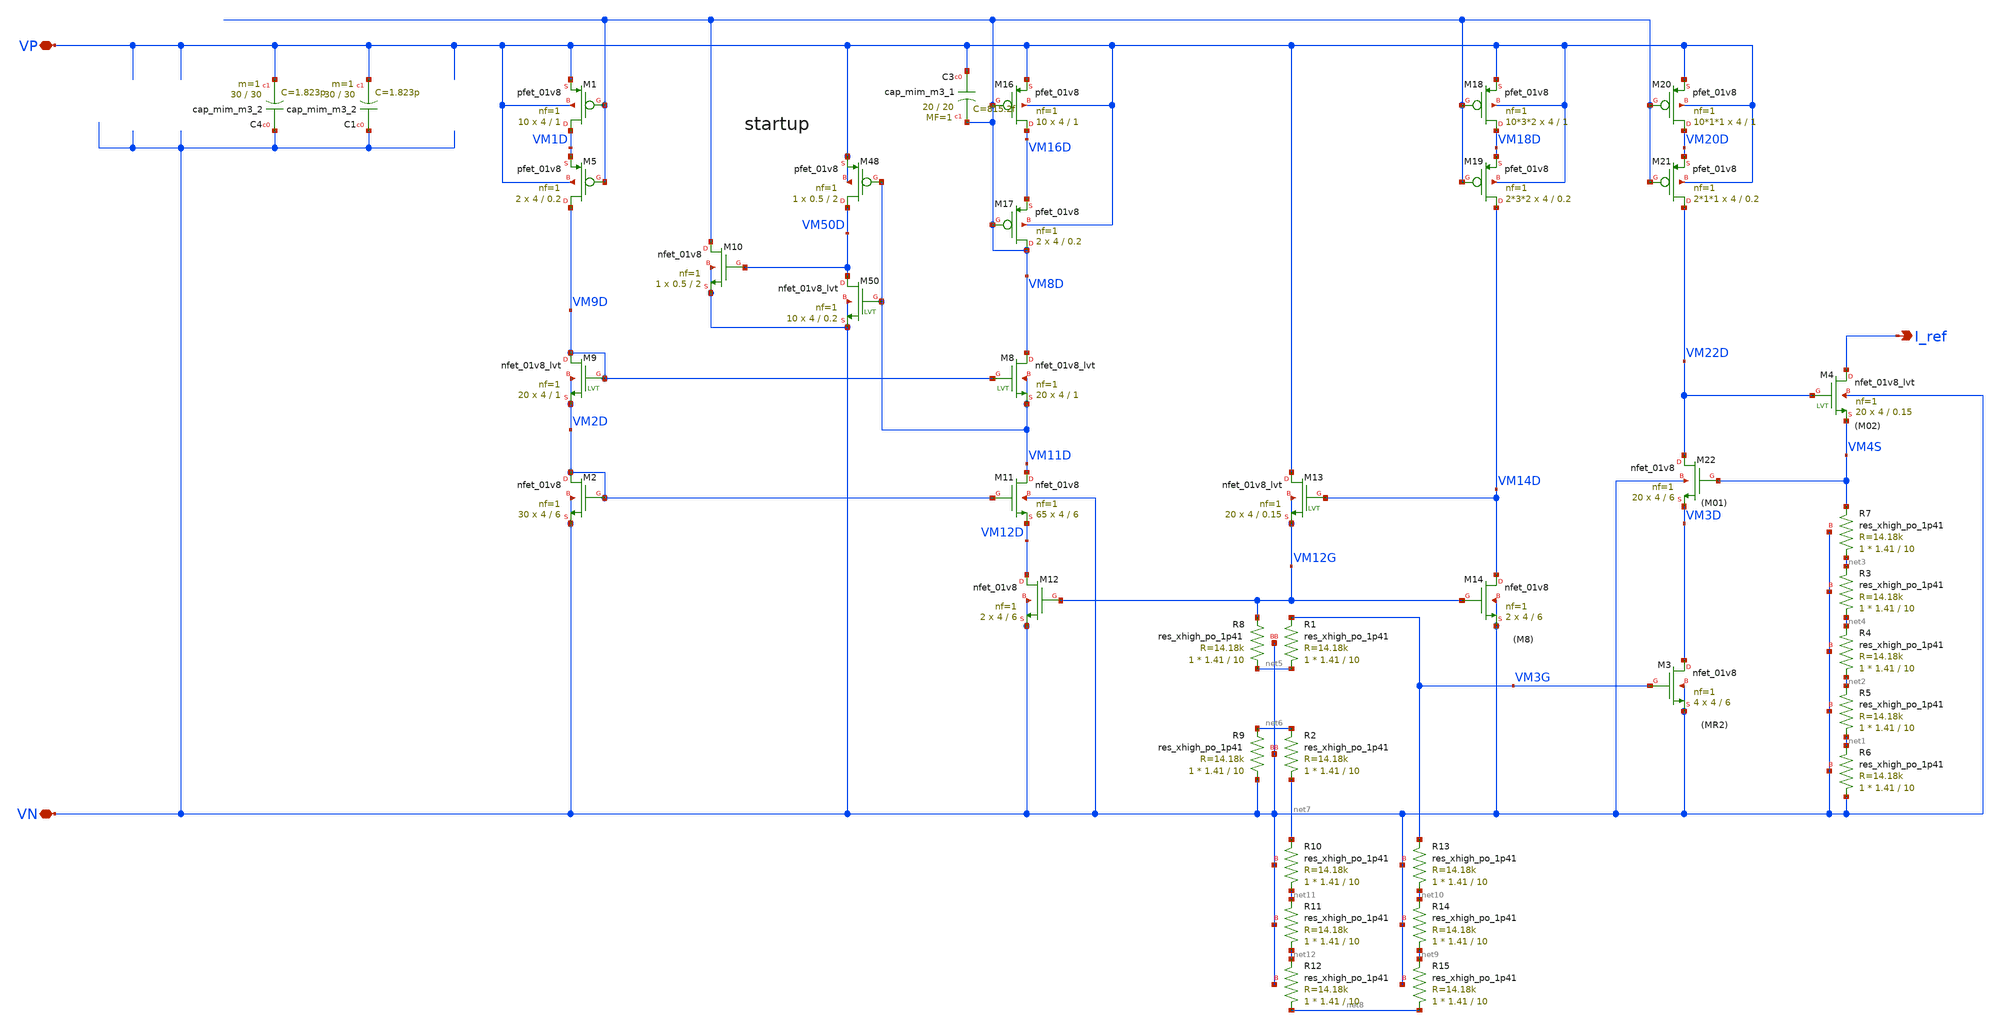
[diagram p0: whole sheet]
** sch_path: xschem/bias/low_pvt_source.sch
**.subckt low_pvt_source VP I_ref VN
*.iopin VP
*.opin I_ref
*.iopin VN
XM1 VM1D VM8D VP VP sky130_fd_pr__pfet_01v8 L=1 W=4 nf=1 ad='int((nf+1)/2) * W/nf * 0.29' as='int((nf+2)/2) * W/nf * 0.29'
+ pd='2*int((nf+1)/2) * (W/nf + 0.29)' ps='2*int((nf+2)/2) * (W/nf + 0.29)' nrd='0.29 / W' nrs='0.29 / W'
+ sa=0 sb=0 sd=0 mult=10 m=10
XM2 VM2D VM2D VN VN sky130_fd_pr__nfet_01v8 L=6 W=4 nf=1 ad='int((nf+1)/2) * W/nf * 0.29' as='int((nf+2)/2) * W/nf * 0.29'
+ pd='2*int((nf+1)/2) * (W/nf + 0.29)' ps='2*int((nf+2)/2) * (W/nf + 0.29)' nrd='0.29 / W' nrs='0.29 / W'
+ sa=0 sb=0 sd=0 mult=30 m=30
XM5 VM9D VM8D VM1D VP sky130_fd_pr__pfet_01v8 L=0.2 W=4 nf=1 ad='int((nf+1)/2) * W/nf * 0.29' as='int((nf+2)/2) * W/nf * 0.29'
+ pd='2*int((nf+1)/2) * (W/nf + 0.29)' ps='2*int((nf+2)/2) * (W/nf + 0.29)' nrd='0.29 / W' nrs='0.29 / W'
+ sa=0 sb=0 sd=0 mult=2 m=2
XM11 VM11D VM2D VM12D VN sky130_fd_pr__nfet_01v8 L=6 W=4 nf=1 ad='int((nf+1)/2) * W/nf * 0.29' as='int((nf+2)/2) * W/nf * 0.29'
+ pd='2*int((nf+1)/2) * (W/nf + 0.29)' ps='2*int((nf+2)/2) * (W/nf + 0.29)' nrd='0.29 / W' nrs='0.29 / W'
+ sa=0 sb=0 sd=0 mult=65 m=65
XM12 VM12D VM12G VN VN sky130_fd_pr__nfet_01v8 L=6 W=4 nf=1 ad='int((nf+1)/2) * W/nf * 0.29' as='int((nf+2)/2) * W/nf * 0.29'
+ pd='2*int((nf+1)/2) * (W/nf + 0.29)' ps='2*int((nf+2)/2) * (W/nf + 0.29)' nrd='0.29 / W' nrs='0.29 / W'
+ sa=0 sb=0 sd=0 mult=2 m=2
XM14 VM14D VM12G VN VN sky130_fd_pr__nfet_01v8 L=6 W=4 nf=1 ad='int((nf+1)/2) * W/nf * 0.29' as='int((nf+2)/2) * W/nf * 0.29'
+ pd='2*int((nf+1)/2) * (W/nf + 0.29)' ps='2*int((nf+2)/2) * (W/nf + 0.29)' nrd='0.29 / W' nrs='0.29 / W'
+ sa=0 sb=0 sd=0 mult=2 m=2
XM16 VM16D VM8D VP VP sky130_fd_pr__pfet_01v8 L=1 W=4 nf=1 ad='int((nf+1)/2) * W/nf * 0.29' as='int((nf+2)/2) * W/nf * 0.29'
+ pd='2*int((nf+1)/2) * (W/nf + 0.29)' ps='2*int((nf+2)/2) * (W/nf + 0.29)' nrd='0.29 / W' nrs='0.29 / W'
+ sa=0 sb=0 sd=0 mult=10 m=10
XM17 VM8D VM8D VM16D VP sky130_fd_pr__pfet_01v8 L=0.2 W=4 nf=1 ad='int((nf+1)/2) * W/nf * 0.29' as='int((nf+2)/2) * W/nf * 0.29'
+ pd='2*int((nf+1)/2) * (W/nf + 0.29)' ps='2*int((nf+2)/2) * (W/nf + 0.29)' nrd='0.29 / W' nrs='0.29 / W'
+ sa=0 sb=0 sd=0 mult=2 m=2
XM18 VM18D VM8D VP VP sky130_fd_pr__pfet_01v8 L=1 W=4 nf=1 ad='int((nf+1)/2) * W/nf * 0.29' as='int((nf+2)/2) * W/nf * 0.29'
+ pd='2*int((nf+1)/2) * (W/nf + 0.29)' ps='2*int((nf+2)/2) * (W/nf + 0.29)' nrd='0.29 / W' nrs='0.29 / W'
+ sa=0 sb=0 sd=0 mult=10*3*2 m=10*3*2
XM19 VM14D VM8D VM18D VP sky130_fd_pr__pfet_01v8 L=0.2 W=4 nf=1 ad='int((nf+1)/2) * W/nf * 0.29' as='int((nf+2)/2) * W/nf * 0.29'
+ pd='2*int((nf+1)/2) * (W/nf + 0.29)' ps='2*int((nf+2)/2) * (W/nf + 0.29)' nrd='0.29 / W' nrs='0.29 / W'
+ sa=0 sb=0 sd=0 mult=2*3*2 m=2*3*2
XM20 VM20D VM8D VP VP sky130_fd_pr__pfet_01v8 L=1 W=4 nf=1 ad='int((nf+1)/2) * W/nf * 0.29' as='int((nf+2)/2) * W/nf * 0.29'
+ pd='2*int((nf+1)/2) * (W/nf + 0.29)' ps='2*int((nf+2)/2) * (W/nf + 0.29)' nrd='0.29 / W' nrs='0.29 / W'
+ sa=0 sb=0 sd=0 mult=10*1*1 m=10*1*1
XM21 VM22D VM8D VM20D VP sky130_fd_pr__pfet_01v8 L=0.2 W=4 nf=1 ad='int((nf+1)/2) * W/nf * 0.29' as='int((nf+2)/2) * W/nf * 0.29'
+ pd='2*int((nf+1)/2) * (W/nf + 0.29)' ps='2*int((nf+2)/2) * (W/nf + 0.29)' nrd='0.29 / W' nrs='0.29 / W'
+ sa=0 sb=0 sd=0 mult=2*1*1 m=2*1*1
XM22 VM22D VM4S VM3D VN sky130_fd_pr__nfet_01v8 L=6 W=4 nf=1 ad='int((nf+1)/2) * W/nf * 0.29' as='int((nf+2)/2) * W/nf * 0.29'
+ pd='2*int((nf+1)/2) * (W/nf + 0.29)' ps='2*int((nf+2)/2) * (W/nf + 0.29)' nrd='0.29 / W' nrs='0.29 / W'
+ sa=0 sb=0 sd=0 mult=20 m=20
XM3 VM3D VM3G VN VN sky130_fd_pr__nfet_01v8 L=6 W=4 nf=1 ad='int((nf+1)/2) * W/nf * 0.29' as='int((nf+2)/2) * W/nf * 0.29'
+ pd='2*int((nf+1)/2) * (W/nf + 0.29)' ps='2*int((nf+2)/2) * (W/nf + 0.29)' nrd='0.29 / W' nrs='0.29 / W'
+ sa=0 sb=0 sd=0 mult=4 m=4
XM13 VP VM14D VM12G VM12G sky130_fd_pr__nfet_01v8_lvt L=0.15 W=4 nf=1 ad='int((nf+1)/2) * W/nf * 0.29'
+ as='int((nf+2)/2) * W/nf * 0.29' pd='2*int((nf+1)/2) * (W/nf + 0.29)' ps='2*int((nf+2)/2) * (W/nf + 0.29)'
+ nrd='0.29 / W' nrs='0.29 / W' sa=0 sb=0 sd=0 mult=20 m=20
XM4 I_ref VM22D VM4S VN sky130_fd_pr__nfet_01v8_lvt L=0.15 W=4 nf=1 ad='int((nf+1)/2) * W/nf * 0.29'
+ as='int((nf+2)/2) * W/nf * 0.29' pd='2*int((nf+1)/2) * (W/nf + 0.29)' ps='2*int((nf+2)/2) * (W/nf + 0.29)'
+ nrd='0.29 / W' nrs='0.29 / W' sa=0 sb=0 sd=0 mult=20 m=20
XM48 VM50D VM11D VP VP sky130_fd_pr__pfet_01v8 L=2 W=0.5 nf=1 ad='int((nf+1)/2) * W/nf * 0.29' as='int((nf+2)/2) * W/nf * 0.29'
+ pd='2*int((nf+1)/2) * (W/nf + 0.29)' ps='2*int((nf+2)/2) * (W/nf + 0.29)' nrd='0.29 / W' nrs='0.29 / W'
+ sa=0 sb=0 sd=0 mult=1 m=1
XM50 VM50D VM11D VN VN sky130_fd_pr__nfet_01v8_lvt L=0.2 W=4 nf=1 ad='int((nf+1)/2) * W/nf * 0.29' as='int((nf+2)/2) * W/nf * 0.29'
+ pd='2*int((nf+1)/2) * (W/nf + 0.29)' ps='2*int((nf+2)/2) * (W/nf + 0.29)' nrd='0.29 / W' nrs='0.29 / W'
+ sa=0 sb=0 sd=0 mult=10 m=10
XC3 VP VM8D sky130_fd_pr__cap_mim_m3_1 W=20 L=20 MF=1 m=1
XM8 VM8D VM9D VM11D VM11D sky130_fd_pr__nfet_01v8_lvt L=1 W=4 nf=1 ad='int((nf+1)/2) * W/nf * 0.29' as='int((nf+2)/2) * W/nf * 0.29'
+ pd='2*int((nf+1)/2) * (W/nf + 0.29)' ps='2*int((nf+2)/2) * (W/nf + 0.29)' nrd='0.29 / W' nrs='0.29 / W'
+ sa=0 sb=0 sd=0 mult=20 m=20
XM9 VM9D VM9D VM2D VM2D sky130_fd_pr__nfet_01v8_lvt L=1 W=4 nf=1 ad='int((nf+1)/2) * W/nf * 0.29' as='int((nf+2)/2) * W/nf * 0.29'
+ pd='2*int((nf+1)/2) * (W/nf + 0.29)' ps='2*int((nf+2)/2) * (W/nf + 0.29)' nrd='0.29 / W' nrs='0.29 / W'
+ sa=0 sb=0 sd=0 mult=20 m=20
XM10 VM8D VM50D VN VN sky130_fd_pr__nfet_01v8 L=2 W=0.5 nf=1 ad='int((nf+1)/2) * W/nf * 0.29' as='int((nf+2)/2) * W/nf * 0.29'
+ pd='2*int((nf+1)/2) * (W/nf + 0.29)' ps='2*int((nf+2)/2) * (W/nf + 0.29)' nrd='0.29 / W' nrs='0.29 / W'
+ sa=0 sb=0 sd=0 mult=1 m=1
XC4 VN VP sky130_fd_pr__cap_mim_m3_2 W=30 L=30 MF=1 m=1
XR7 net3 VM4S VN sky130_fd_pr__res_xhigh_po_1p41 L=10 mult=1 m=1
XR3 net4 net3 VN sky130_fd_pr__res_xhigh_po_1p41 L=10 mult=1 m=1
XR4 net2 net4 VN sky130_fd_pr__res_xhigh_po_1p41 L=10 mult=1 m=1
XR5 net1 net2 VN sky130_fd_pr__res_xhigh_po_1p41 L=10 mult=1 m=1
XR6 VN net1 VN sky130_fd_pr__res_xhigh_po_1p41 L=10 mult=1 m=1
XR8 net5 VM12G VN sky130_fd_pr__res_xhigh_po_1p41 L=10 mult=1 m=1
XR1 net5 VM3G VN sky130_fd_pr__res_xhigh_po_1p41 L=10 mult=1 m=1
XR2 net7 net6 VN sky130_fd_pr__res_xhigh_po_1p41 L=10 mult=1 m=1
XR9 VN net6 VN sky130_fd_pr__res_xhigh_po_1p41 L=10 mult=1 m=1
XR10 net11 net7 VN sky130_fd_pr__res_xhigh_po_1p41 L=10 mult=1 m=1
XR11 net12 net11 VN sky130_fd_pr__res_xhigh_po_1p41 L=10 mult=1 m=1
XR12 net8 net12 VN sky130_fd_pr__res_xhigh_po_1p41 L=10 mult=1 m=1
XR13 net10 VM3G VN sky130_fd_pr__res_xhigh_po_1p41 L=10 mult=1 m=1
XR14 net9 net10 VN sky130_fd_pr__res_xhigh_po_1p41 L=10 mult=1 m=1
XR15 net8 net9 VN sky130_fd_pr__res_xhigh_po_1p41 L=10 mult=1 m=1
XC1 VN VP sky130_fd_pr__cap_mim_m3_2 W=30 L=30 MF=1 m=1
**.ends
.end
